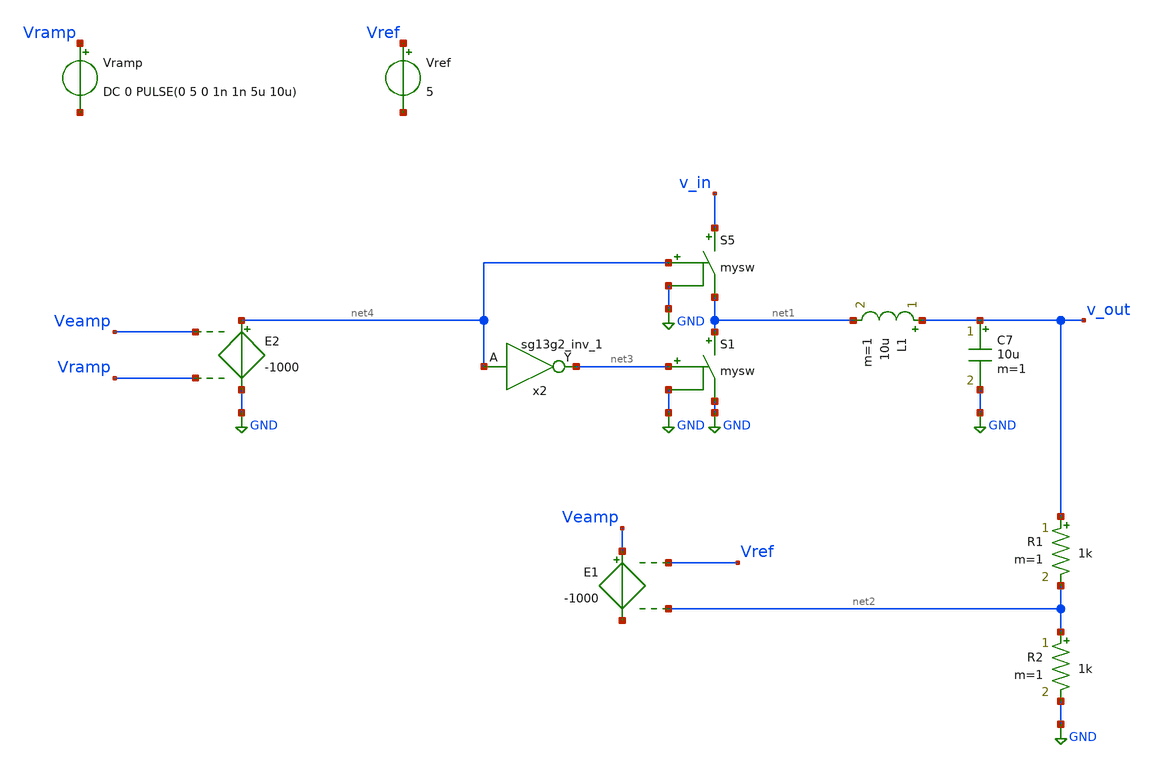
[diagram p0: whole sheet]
** sch_path: Designs/ideal_circuits/ideal_dcdc.sch
**.subckt ideal_dcdc
Vramp Vramp net5 DC 0 PULSE(0 5 0 1n 1n 5u 10u)
S5 v_in net1 net4 GND mysw
S1 net1 GND net3 GND mysw
L1 v_out net1 10u m=1
C7 v_out GND 10u m=1
R1 v_out net2 1k m=1
R2 net2 GND 1k m=1
Vref Vref net6 5
E1 Veamp net7 Vref net2 -1000
x2 net3 net4 1.5 0 sg13g2_inv_1
E2 net4 GND Veamp Vramp -1000
**.ends

* expanding   symbol:  sg13g2_stdcells/sg13g2_inv_1.sym # of pins=2
** sym_path: sg13g2_stdcells/sg13g2_inv_1.sym
** sch_path: sg13g2_stdcells/sg13g2_inv_1.sch
.subckt sg13g2_inv_1 Y A VDD VSS
*.opin Y
*.ipin A
*.iopin VDD
*.iopin VSS
XM1 Y A VSS VSS sg13_lv_nmos w=740.00n l=130.00n ng=1 m=1 mm_ok=1
XM2 Y A VDD VDD sg13_lv_pmos w=1.12u l=130.00n ng=1 m=1 mm_ok=1
.ends

.GLOBAL GND
.end
